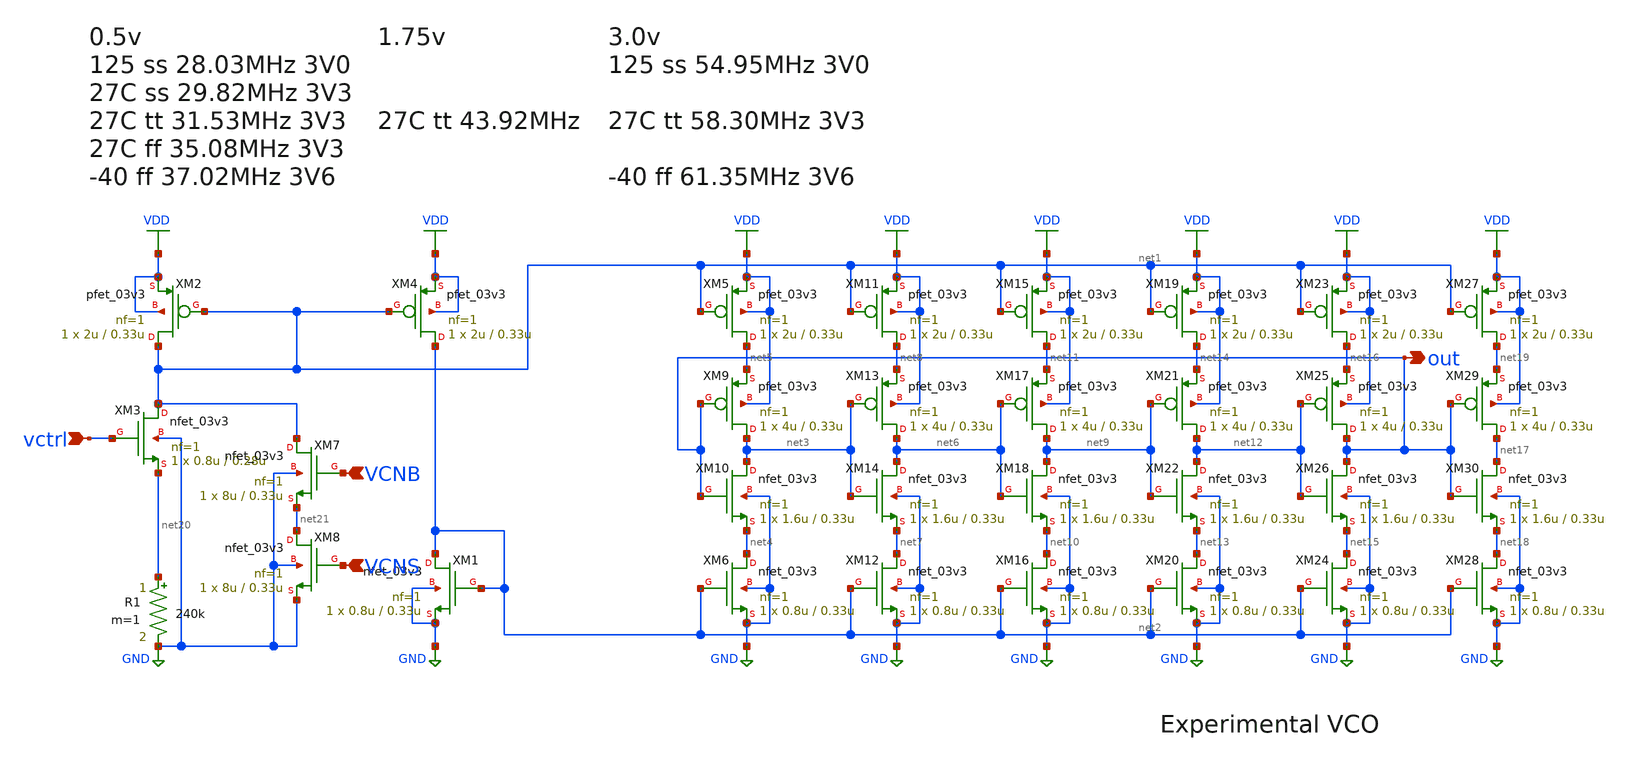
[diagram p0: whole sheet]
** sch_path: schematic/vco.sch
**.subckt vco vctrl out VCNB VCNS
*.ipin vctrl
*.opin out
*.ipin VCNB
*.ipin VCNS
XM2 net1 net1 VDD VDD pfet_03v3 L=0.33u W=2u nf=1 ad='int((nf+1)/2) * W/nf * 0.18u' as='int((nf+2)/2) * W/nf * 0.18u'
+ pd='2*int((nf+1)/2) * (W/nf + 0.18u)' ps='2*int((nf+2)/2) * (W/nf + 0.18u)' nrd='0.18u / W' nrs='0.18u / W'
+ sa=0 sb=0 sd=0 m=1
XM4 net2 net1 VDD VDD pfet_03v3 L=0.33u W=2u nf=1 ad='int((nf+1)/2) * W/nf * 0.18u' as='int((nf+2)/2) * W/nf * 0.18u'
+ pd='2*int((nf+1)/2) * (W/nf + 0.18u)' ps='2*int((nf+2)/2) * (W/nf + 0.18u)' nrd='0.18u / W' nrs='0.18u / W'
+ sa=0 sb=0 sd=0 m=1
XM1 net2 net2 GND GND nfet_03v3 L=0.33u W=0.8u nf=1 ad='int((nf+1)/2) * W/nf * 0.18u' as='int((nf+2)/2) * W/nf * 0.18u'
+ pd='2*int((nf+1)/2) * (W/nf + 0.18u)' ps='2*int((nf+2)/2) * (W/nf + 0.18u)' nrd='0.18u / W' nrs='0.18u / W'
+ sa=0 sb=0 sd=0 m=1
XM5 net5 net1 VDD VDD pfet_03v3 L=0.33u W=2u nf=1 ad='int((nf+1)/2) * W/nf * 0.18u' as='int((nf+2)/2) * W/nf * 0.18u'
+ pd='2*int((nf+1)/2) * (W/nf + 0.18u)' ps='2*int((nf+2)/2) * (W/nf + 0.18u)' nrd='0.18u / W' nrs='0.18u / W'
+ sa=0 sb=0 sd=0 m=1
XM6 net4 net2 GND GND nfet_03v3 L=0.33u W=0.8u nf=1 ad='int((nf+1)/2) * W/nf * 0.18u' as='int((nf+2)/2) * W/nf * 0.18u'
+ pd='2*int((nf+1)/2) * (W/nf + 0.18u)' ps='2*int((nf+2)/2) * (W/nf + 0.18u)' nrd='0.18u / W' nrs='0.18u / W'
+ sa=0 sb=0 sd=0 m=1
R1 net20 GND 240k m=1
XM3 net1 vctrl net20 GND nfet_03v3 L=0.28u W=0.8u nf=1 ad='int((nf+1)/2) * W/nf * 0.18u' as='int((nf+2)/2) * W/nf * 0.18u'
+ pd='2*int((nf+1)/2) * (W/nf + 0.18u)' ps='2*int((nf+2)/2) * (W/nf + 0.18u)' nrd='0.18u / W' nrs='0.18u / W'
+ sa=0 sb=0 sd=0 m=1
XM9 net3 out net5 VDD pfet_03v3 L=0.33u W=4u nf=1 ad='int((nf+1)/2) * W/nf * 0.18u' as='int((nf+2)/2) * W/nf * 0.18u'
+ pd='2*int((nf+1)/2) * (W/nf + 0.18u)' ps='2*int((nf+2)/2) * (W/nf + 0.18u)' nrd='0.18u / W' nrs='0.18u / W'
+ sa=0 sb=0 sd=0 m=1
XM10 net3 out net4 GND nfet_03v3 L=0.33u W=1.6u nf=1 ad='int((nf+1)/2) * W/nf * 0.18u' as='int((nf+2)/2) * W/nf * 0.18u'
+ pd='2*int((nf+1)/2) * (W/nf + 0.18u)' ps='2*int((nf+2)/2) * (W/nf + 0.18u)' nrd='0.18u / W' nrs='0.18u / W'
+ sa=0 sb=0 sd=0 m=1
XM11 net8 net1 VDD VDD pfet_03v3 L=0.33u W=2u nf=1 ad='int((nf+1)/2) * W/nf * 0.18u' as='int((nf+2)/2) * W/nf * 0.18u'
+ pd='2*int((nf+1)/2) * (W/nf + 0.18u)' ps='2*int((nf+2)/2) * (W/nf + 0.18u)' nrd='0.18u / W' nrs='0.18u / W'
+ sa=0 sb=0 sd=0 m=1
XM12 net7 net2 GND GND nfet_03v3 L=0.33u W=0.8u nf=1 ad='int((nf+1)/2) * W/nf * 0.18u' as='int((nf+2)/2) * W/nf * 0.18u'
+ pd='2*int((nf+1)/2) * (W/nf + 0.18u)' ps='2*int((nf+2)/2) * (W/nf + 0.18u)' nrd='0.18u / W' nrs='0.18u / W'
+ sa=0 sb=0 sd=0 m=1
XM13 net6 net3 net8 VDD pfet_03v3 L=0.33u W=4u nf=1 ad='int((nf+1)/2) * W/nf * 0.18u' as='int((nf+2)/2) * W/nf * 0.18u'
+ pd='2*int((nf+1)/2) * (W/nf + 0.18u)' ps='2*int((nf+2)/2) * (W/nf + 0.18u)' nrd='0.18u / W' nrs='0.18u / W'
+ sa=0 sb=0 sd=0 m=1
XM14 net6 net3 net7 GND nfet_03v3 L=0.33u W=1.6u nf=1 ad='int((nf+1)/2) * W/nf * 0.18u' as='int((nf+2)/2) * W/nf * 0.18u'
+ pd='2*int((nf+1)/2) * (W/nf + 0.18u)' ps='2*int((nf+2)/2) * (W/nf + 0.18u)' nrd='0.18u / W' nrs='0.18u / W'
+ sa=0 sb=0 sd=0 m=1
XM15 net11 net1 VDD VDD pfet_03v3 L=0.33u W=2u nf=1 ad='int((nf+1)/2) * W/nf * 0.18u' as='int((nf+2)/2) * W/nf * 0.18u'
+ pd='2*int((nf+1)/2) * (W/nf + 0.18u)' ps='2*int((nf+2)/2) * (W/nf + 0.18u)' nrd='0.18u / W' nrs='0.18u / W'
+ sa=0 sb=0 sd=0 m=1
XM16 net10 net2 GND GND nfet_03v3 L=0.33u W=0.8u nf=1 ad='int((nf+1)/2) * W/nf * 0.18u' as='int((nf+2)/2) * W/nf * 0.18u'
+ pd='2*int((nf+1)/2) * (W/nf + 0.18u)' ps='2*int((nf+2)/2) * (W/nf + 0.18u)' nrd='0.18u / W' nrs='0.18u / W'
+ sa=0 sb=0 sd=0 m=1
XM17 net9 net6 net11 VDD pfet_03v3 L=0.33u W=4u nf=1 ad='int((nf+1)/2) * W/nf * 0.18u' as='int((nf+2)/2) * W/nf * 0.18u'
+ pd='2*int((nf+1)/2) * (W/nf + 0.18u)' ps='2*int((nf+2)/2) * (W/nf + 0.18u)' nrd='0.18u / W' nrs='0.18u / W'
+ sa=0 sb=0 sd=0 m=1
XM18 net9 net6 net10 GND nfet_03v3 L=0.33u W=1.6u nf=1 ad='int((nf+1)/2) * W/nf * 0.18u' as='int((nf+2)/2) * W/nf * 0.18u'
+ pd='2*int((nf+1)/2) * (W/nf + 0.18u)' ps='2*int((nf+2)/2) * (W/nf + 0.18u)' nrd='0.18u / W' nrs='0.18u / W'
+ sa=0 sb=0 sd=0 m=1
XM19 net14 net1 VDD VDD pfet_03v3 L=0.33u W=2u nf=1 ad='int((nf+1)/2) * W/nf * 0.18u' as='int((nf+2)/2) * W/nf * 0.18u'
+ pd='2*int((nf+1)/2) * (W/nf + 0.18u)' ps='2*int((nf+2)/2) * (W/nf + 0.18u)' nrd='0.18u / W' nrs='0.18u / W'
+ sa=0 sb=0 sd=0 m=1
XM20 net13 net2 GND GND nfet_03v3 L=0.33u W=0.8u nf=1 ad='int((nf+1)/2) * W/nf * 0.18u' as='int((nf+2)/2) * W/nf * 0.18u'
+ pd='2*int((nf+1)/2) * (W/nf + 0.18u)' ps='2*int((nf+2)/2) * (W/nf + 0.18u)' nrd='0.18u / W' nrs='0.18u / W'
+ sa=0 sb=0 sd=0 m=1
XM21 net12 net9 net14 VDD pfet_03v3 L=0.33u W=4u nf=1 ad='int((nf+1)/2) * W/nf * 0.18u' as='int((nf+2)/2) * W/nf * 0.18u'
+ pd='2*int((nf+1)/2) * (W/nf + 0.18u)' ps='2*int((nf+2)/2) * (W/nf + 0.18u)' nrd='0.18u / W' nrs='0.18u / W'
+ sa=0 sb=0 sd=0 m=1
XM22 net12 net9 net13 GND nfet_03v3 L=0.33u W=1.6u nf=1 ad='int((nf+1)/2) * W/nf * 0.18u' as='int((nf+2)/2) * W/nf * 0.18u'
+ pd='2*int((nf+1)/2) * (W/nf + 0.18u)' ps='2*int((nf+2)/2) * (W/nf + 0.18u)' nrd='0.18u / W' nrs='0.18u / W'
+ sa=0 sb=0 sd=0 m=1
XM23 net16 net1 VDD VDD pfet_03v3 L=0.33u W=2u nf=1 ad='int((nf+1)/2) * W/nf * 0.18u' as='int((nf+2)/2) * W/nf * 0.18u'
+ pd='2*int((nf+1)/2) * (W/nf + 0.18u)' ps='2*int((nf+2)/2) * (W/nf + 0.18u)' nrd='0.18u / W' nrs='0.18u / W'
+ sa=0 sb=0 sd=0 m=1
XM24 net15 net2 GND GND nfet_03v3 L=0.33u W=0.8u nf=1 ad='int((nf+1)/2) * W/nf * 0.18u' as='int((nf+2)/2) * W/nf * 0.18u'
+ pd='2*int((nf+1)/2) * (W/nf + 0.18u)' ps='2*int((nf+2)/2) * (W/nf + 0.18u)' nrd='0.18u / W' nrs='0.18u / W'
+ sa=0 sb=0 sd=0 m=1
XM25 out net12 net16 VDD pfet_03v3 L=0.33u W=4u nf=1 ad='int((nf+1)/2) * W/nf * 0.18u' as='int((nf+2)/2) * W/nf * 0.18u'
+ pd='2*int((nf+1)/2) * (W/nf + 0.18u)' ps='2*int((nf+2)/2) * (W/nf + 0.18u)' nrd='0.18u / W' nrs='0.18u / W'
+ sa=0 sb=0 sd=0 m=1
XM26 out net12 net15 GND nfet_03v3 L=0.33u W=1.6u nf=1 ad='int((nf+1)/2) * W/nf * 0.18u' as='int((nf+2)/2) * W/nf * 0.18u'
+ pd='2*int((nf+1)/2) * (W/nf + 0.18u)' ps='2*int((nf+2)/2) * (W/nf + 0.18u)' nrd='0.18u / W' nrs='0.18u / W'
+ sa=0 sb=0 sd=0 m=1
XM27 net19 net1 VDD VDD pfet_03v3 L=0.33u W=2u nf=1 ad='int((nf+1)/2) * W/nf * 0.18u' as='int((nf+2)/2) * W/nf * 0.18u'
+ pd='2*int((nf+1)/2) * (W/nf + 0.18u)' ps='2*int((nf+2)/2) * (W/nf + 0.18u)' nrd='0.18u / W' nrs='0.18u / W'
+ sa=0 sb=0 sd=0 m=1
XM28 net18 net2 GND GND nfet_03v3 L=0.33u W=0.8u nf=1 ad='int((nf+1)/2) * W/nf * 0.18u' as='int((nf+2)/2) * W/nf * 0.18u'
+ pd='2*int((nf+1)/2) * (W/nf + 0.18u)' ps='2*int((nf+2)/2) * (W/nf + 0.18u)' nrd='0.18u / W' nrs='0.18u / W'
+ sa=0 sb=0 sd=0 m=1
XM29 net17 out net19 VDD pfet_03v3 L=0.33u W=4u nf=1 ad='int((nf+1)/2) * W/nf * 0.18u' as='int((nf+2)/2) * W/nf * 0.18u'
+ pd='2*int((nf+1)/2) * (W/nf + 0.18u)' ps='2*int((nf+2)/2) * (W/nf + 0.18u)' nrd='0.18u / W' nrs='0.18u / W'
+ sa=0 sb=0 sd=0 m=1
XM30 net17 out net18 GND nfet_03v3 L=0.33u W=1.6u nf=1 ad='int((nf+1)/2) * W/nf * 0.18u' as='int((nf+2)/2) * W/nf * 0.18u'
+ pd='2*int((nf+1)/2) * (W/nf + 0.18u)' ps='2*int((nf+2)/2) * (W/nf + 0.18u)' nrd='0.18u / W' nrs='0.18u / W'
+ sa=0 sb=0 sd=0 m=1
XM7 net1 VCNB net21 GND nfet_03v3 L=0.33u W=8u nf=1 ad='int((nf+1)/2) * W/nf * 0.18u' as='int((nf+2)/2) * W/nf * 0.18u'
+ pd='2*int((nf+1)/2) * (W/nf + 0.18u)' ps='2*int((nf+2)/2) * (W/nf + 0.18u)' nrd='0.18u / W' nrs='0.18u / W'
+ sa=0 sb=0 sd=0 m=1
XM8 net21 VCNS GND GND nfet_03v3 L=0.33u W=8u nf=1 ad='int((nf+1)/2) * W/nf * 0.18u' as='int((nf+2)/2) * W/nf * 0.18u'
+ pd='2*int((nf+1)/2) * (W/nf + 0.18u)' ps='2*int((nf+2)/2) * (W/nf + 0.18u)' nrd='0.18u / W' nrs='0.18u / W'
+ sa=0 sb=0 sd=0 m=1
**.ends
.GLOBAL GND
.GLOBAL VDD
.end
